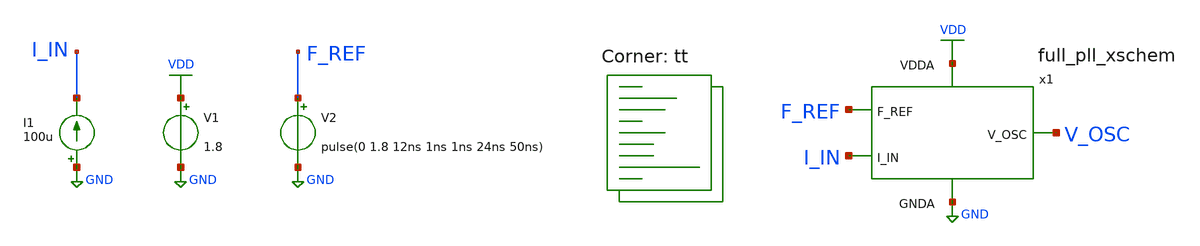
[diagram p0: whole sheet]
** sch_path: projects/pll/full_pll/magic/tb_full_pll_xschem.sch
**.subckt tb_full_pll_xschem
V1 VDD GND 1.8
V2 F_REF GND pulse(0 1.8 12ns 1ns 1ns 24ns 50ns)
I1 GND I_IN 100u
x1 V_OSC VDD GND F_REF I_IN full_pll_xschem
**** begin user architecture code
.lib $::SKYWATER_MODELS/sky130.lib.spice tt



* .include /foss/designs/my_design/projects/pll/charge_pump/magic/pfd_cp_input_magic.spice
* .include /foss/designs/my_design/projects/pll/charge_pump/magic/charge_pump_magic.spice
* .include /foss/designs/my_design/projects/pll/charge_pump/magic/rail_to_rail_opamp_magic.spice
* .include /foss/designs/my_design/projects/pll/charge_pump/magic/loop_filter_magic.spice

.option method=gear
.option wnflag=1
**.option savecurrents


* V_out initial voltage

.ic v(x1.v_cont) = 0.0

.control
  save v(v_osc) v(x1.v_cont) v(x1.f_vco) v(x1.up_pfd) v(x1.down_pfd) v(x1.up_input) v(x1.down_input)
+ v(x1.x)
  * save all

  * timestep for exact simulation results
  * tran 5ps 0.5us

  * timestep for faster simulation results
  tran 5ps 6us

  remzerovec
  write tb_full_pll_xschem.raw
  set appendwrite

.endc



**** end user architecture code
**.ends
.GLOBAL GND
.GLOBAL VDD
.end
